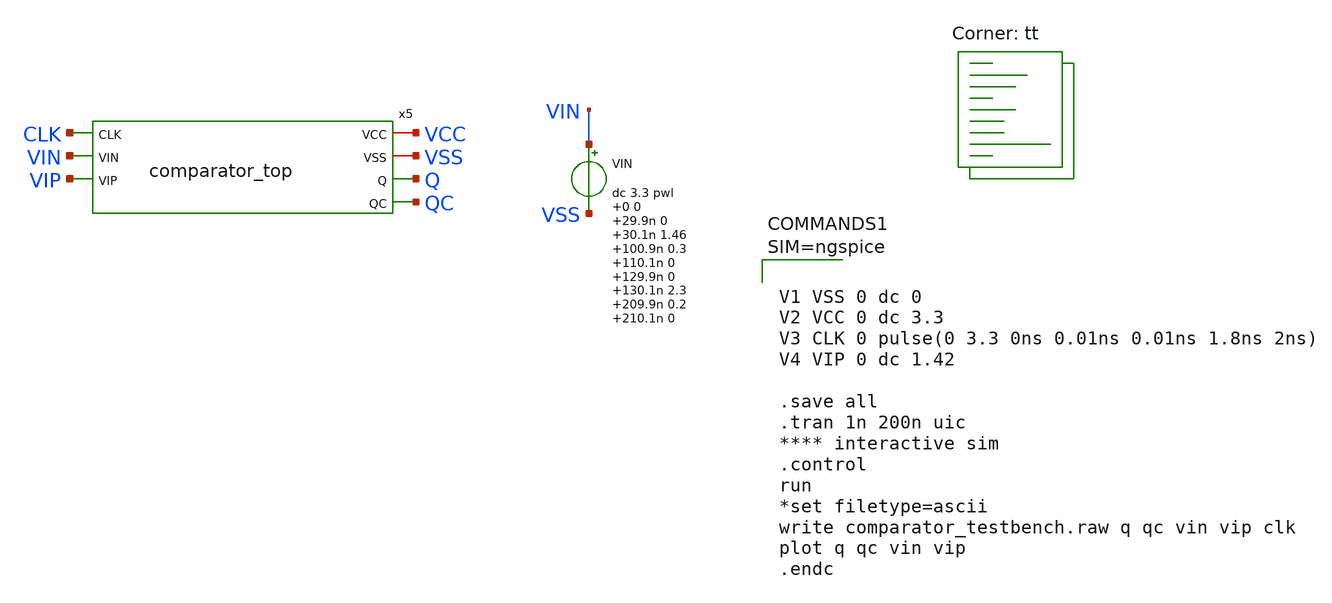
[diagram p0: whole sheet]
** sch_path: Comparator/schematic/miyahara/comparator_testbench.sch
**.subckt comparator_testbench
VIN VIN VSS dc 3.3 pwl 0 0 29.9n 0 30.1n 1.46 100.9n 0.3 110.1n 0 129.9n 0 130.1n 2.3 209.9n 0.2
+ 210.1n 0
x5 VCC VSS CLK VIN VIP Q QC comparator_top
**** begin user architecture code
.lib $::SKYWATER_MODELS/sky130.lib.spice tt



V1 VSS 0 dc 0
V2 VCC 0 dc 3.3
V3 CLK 0 pulse(0 3.3 0ns 0.01ns 0.01ns 1.8ns 2ns)
V4 VIP 0 dc 1.42

.save all
.tran 1n 200n uic
**** interactive sim
.control
run
*set filetype=ascii
write comparator_testbench.raw q qc vin vip clk
plot q qc vin vip
.endc



**** end user architecture code
**.ends
.end
